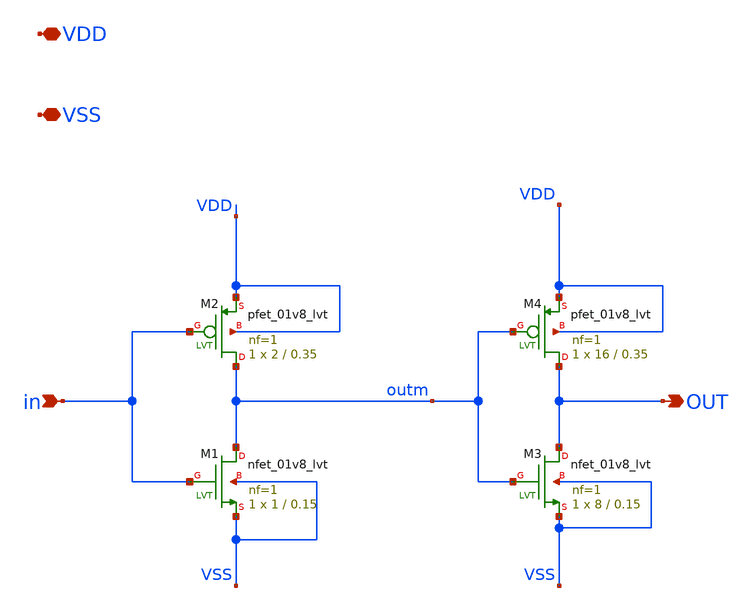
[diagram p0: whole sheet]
** sch_path: xschem/inverter.sch
**.subckt inverter VDD VSS in OUT
*.iopin VDD
*.iopin VSS
*.ipin in
*.opin OUT
XM1 outm in VSS VSS sky130_fd_pr__nfet_01v8_lvt L=0.15 W=1 nf=1 ad='int((nf+1)/2) * W/nf * 0.29' as='int((nf+2)/2) * W/nf * 0.29'
+ pd='2*int((nf+1)/2) * (W/nf + 0.29)' ps='2*int((nf+2)/2) * (W/nf + 0.29)' nrd='0.29 / W' nrs='0.29 / W'
+ sa=0 sb=0 sd=0 mult=1 m=1
XM2 outm in VDD VDD sky130_fd_pr__pfet_01v8_lvt L=0.35 W=2 nf=1 ad='int((nf+1)/2) * W/nf * 0.29' as='int((nf+2)/2) * W/nf * 0.29'
+ pd='2*int((nf+1)/2) * (W/nf + 0.29)' ps='2*int((nf+2)/2) * (W/nf + 0.29)' nrd='0.29 / W' nrs='0.29 / W'
+ sa=0 sb=0 sd=0 mult=1 m=1
XM3 OUT outm VSS VSS sky130_fd_pr__nfet_01v8_lvt L=0.15 W=8 nf=1 ad='int((nf+1)/2) * W/nf * 0.29' as='int((nf+2)/2) * W/nf * 0.29'
+ pd='2*int((nf+1)/2) * (W/nf + 0.29)' ps='2*int((nf+2)/2) * (W/nf + 0.29)' nrd='0.29 / W' nrs='0.29 / W'
+ sa=0 sb=0 sd=0 mult=1 m=1
XM4 OUT outm VDD VDD sky130_fd_pr__pfet_01v8_lvt L=0.35 W=16 nf=1 ad='int((nf+1)/2) * W/nf * 0.29' as='int((nf+2)/2) * W/nf * 0.29'
+ pd='2*int((nf+1)/2) * (W/nf + 0.29)' ps='2*int((nf+2)/2) * (W/nf + 0.29)' nrd='0.29 / W' nrs='0.29 / W'
+ sa=0 sb=0 sd=0 mult=1 m=1
**.ends
.end
